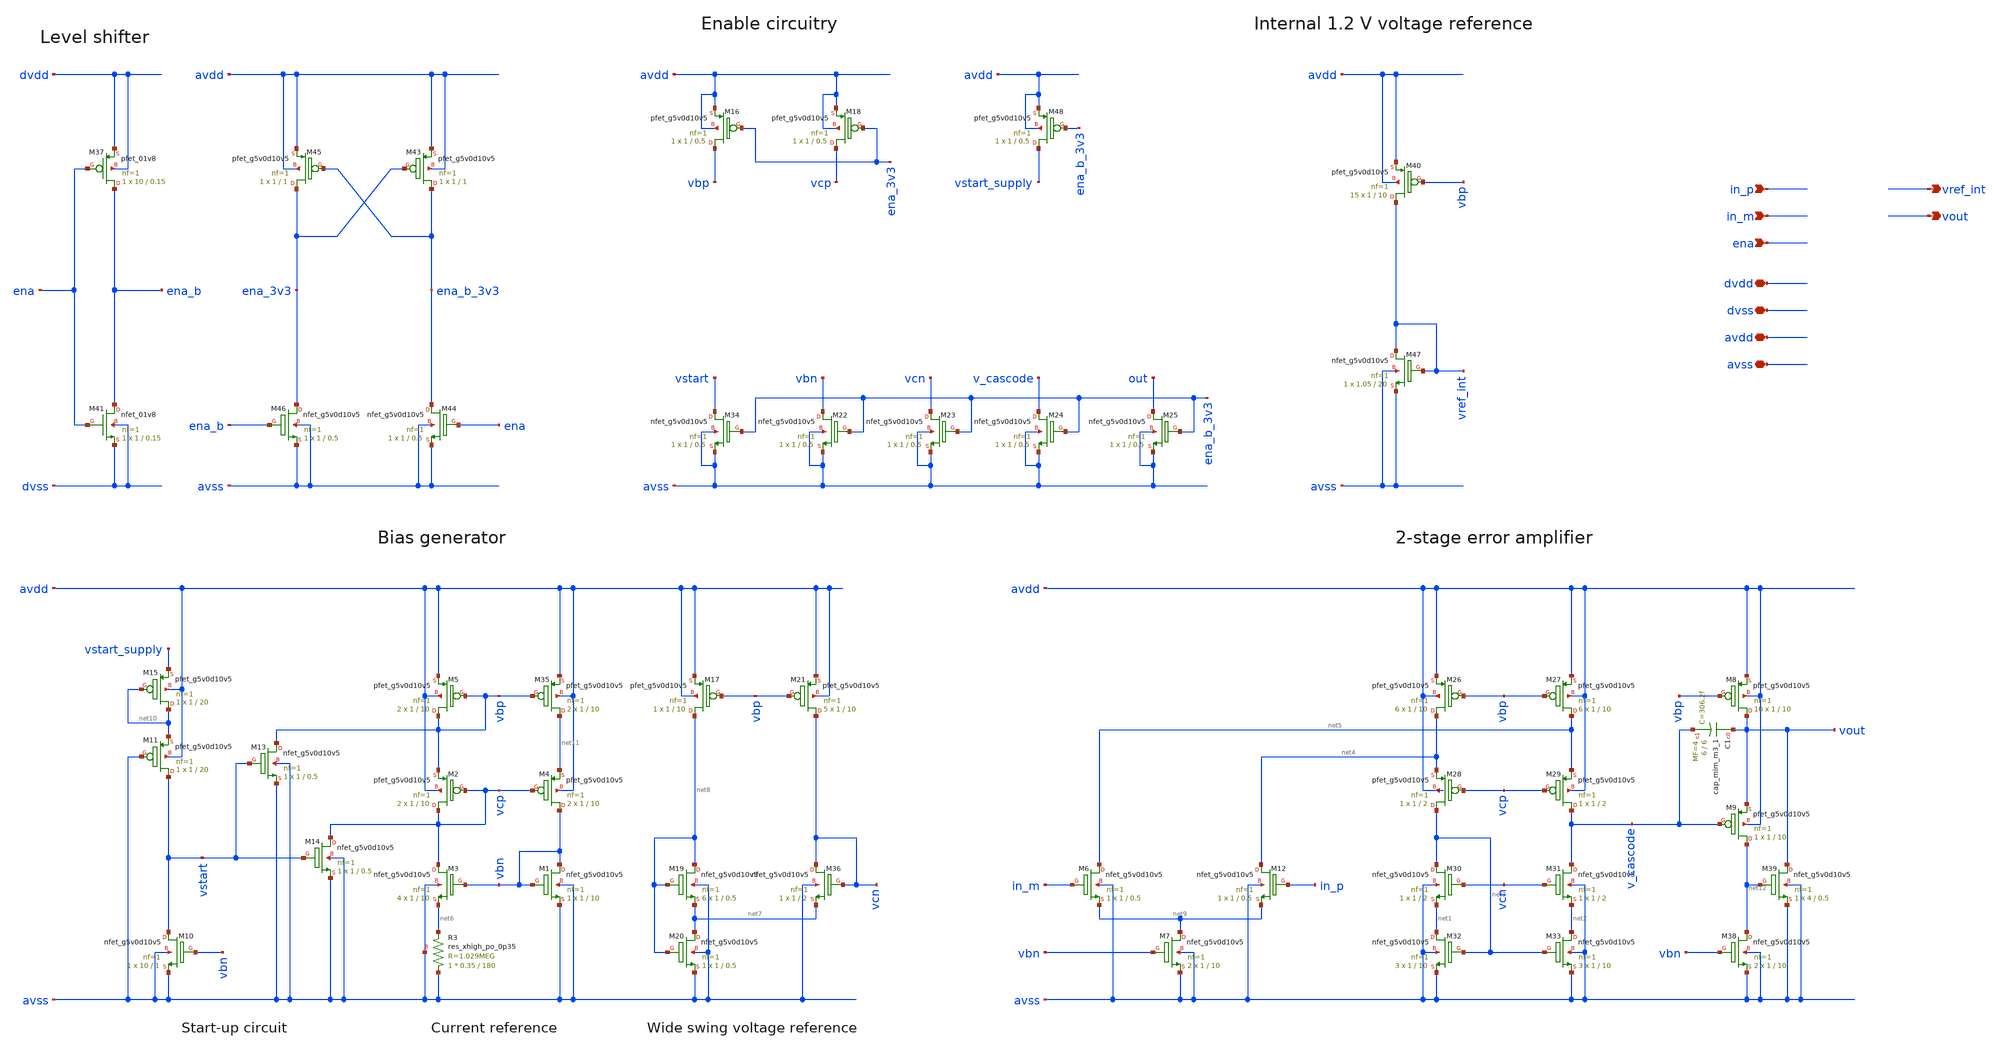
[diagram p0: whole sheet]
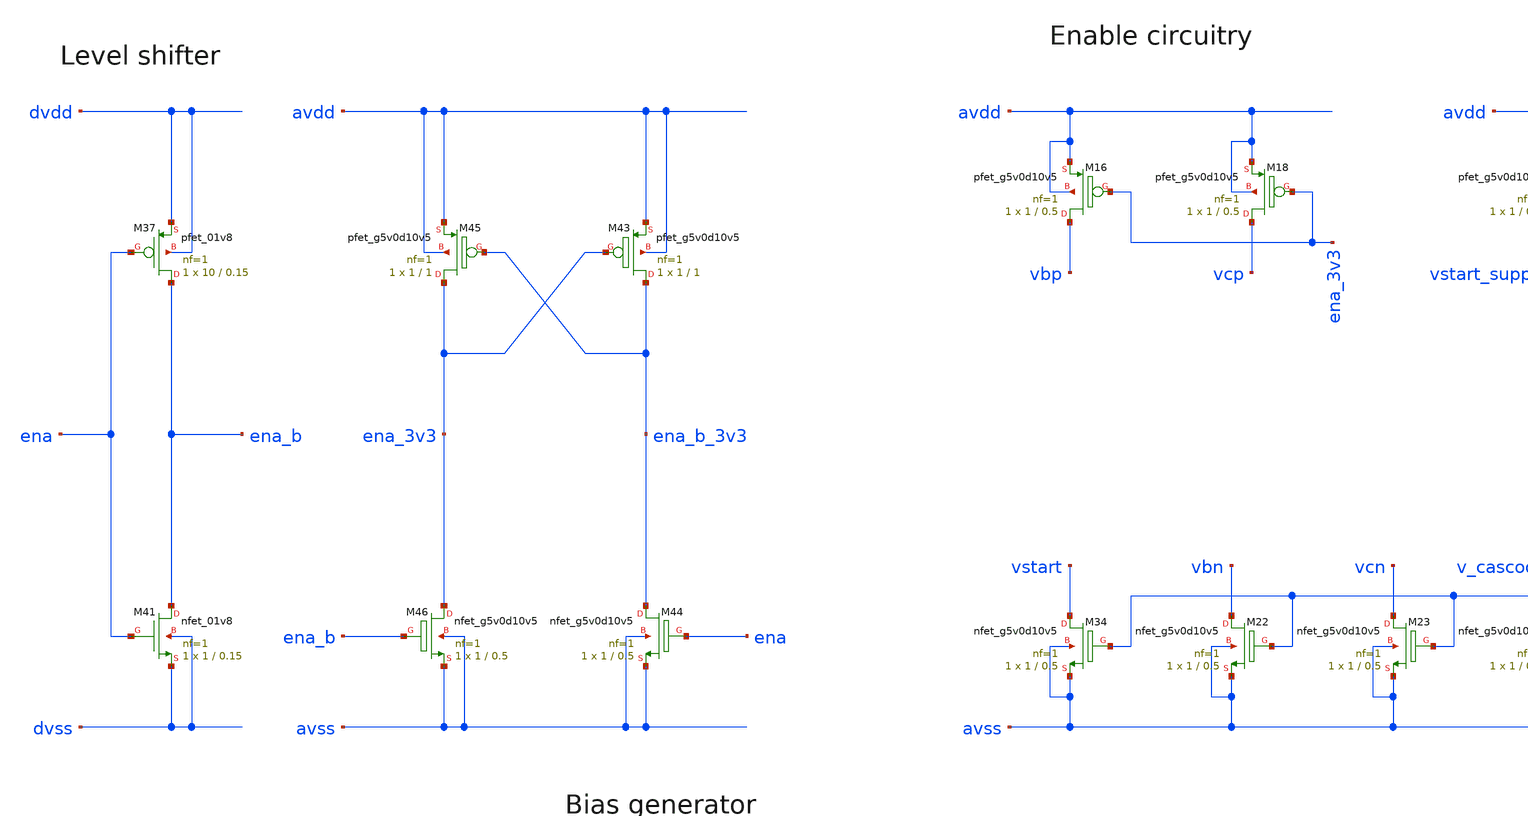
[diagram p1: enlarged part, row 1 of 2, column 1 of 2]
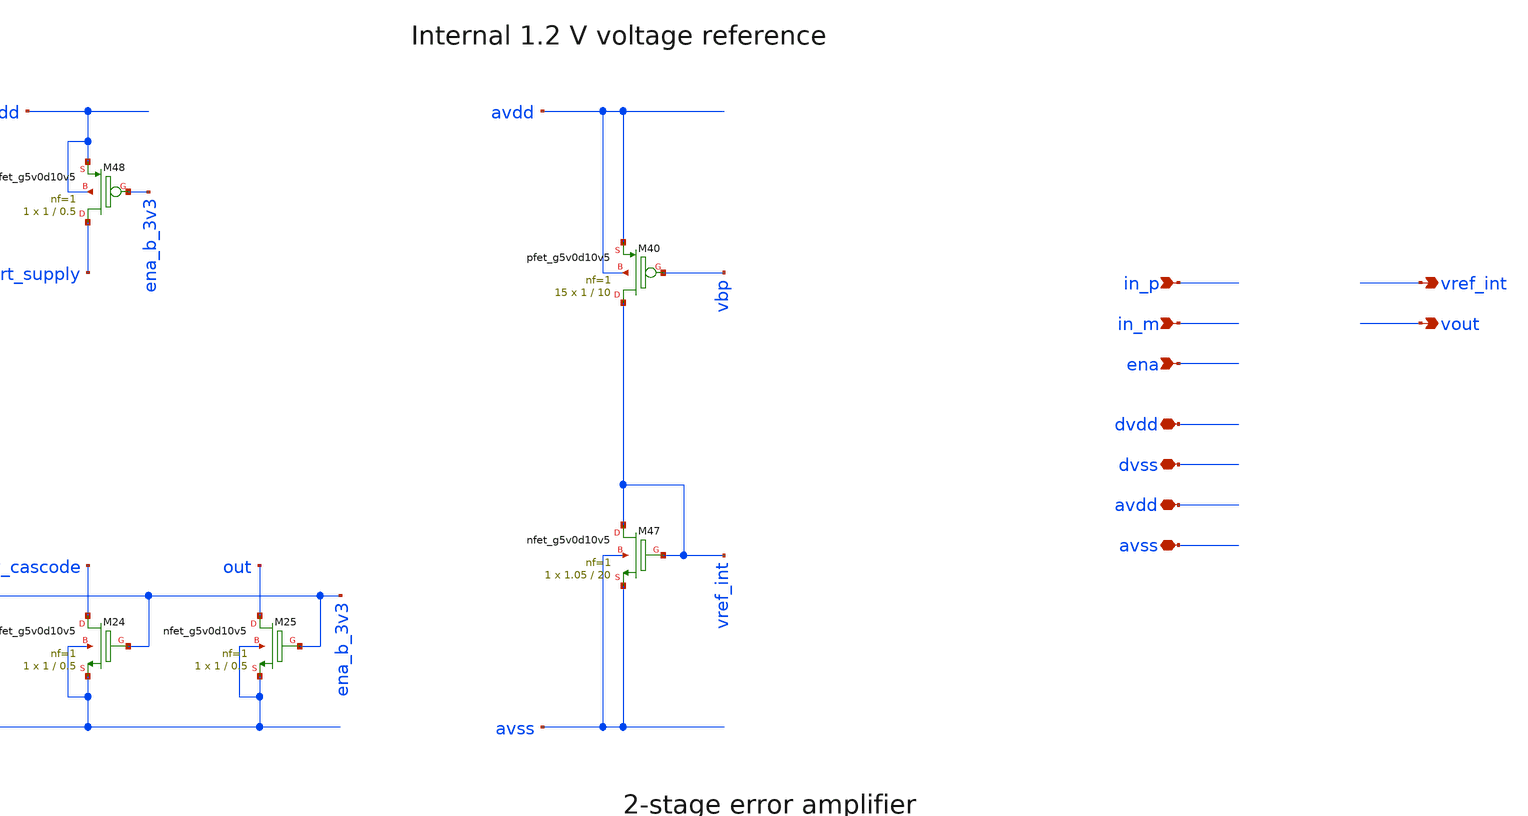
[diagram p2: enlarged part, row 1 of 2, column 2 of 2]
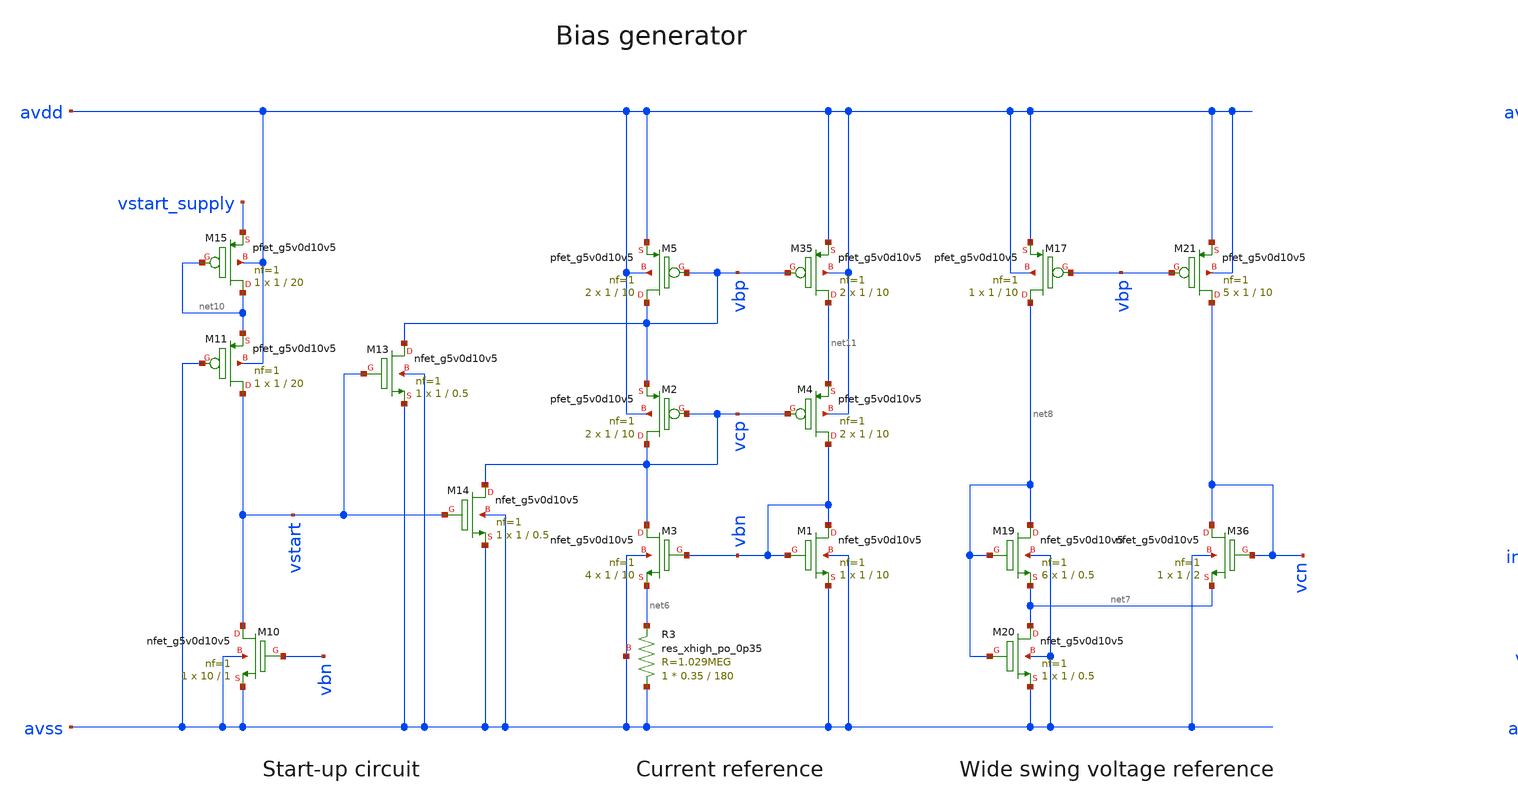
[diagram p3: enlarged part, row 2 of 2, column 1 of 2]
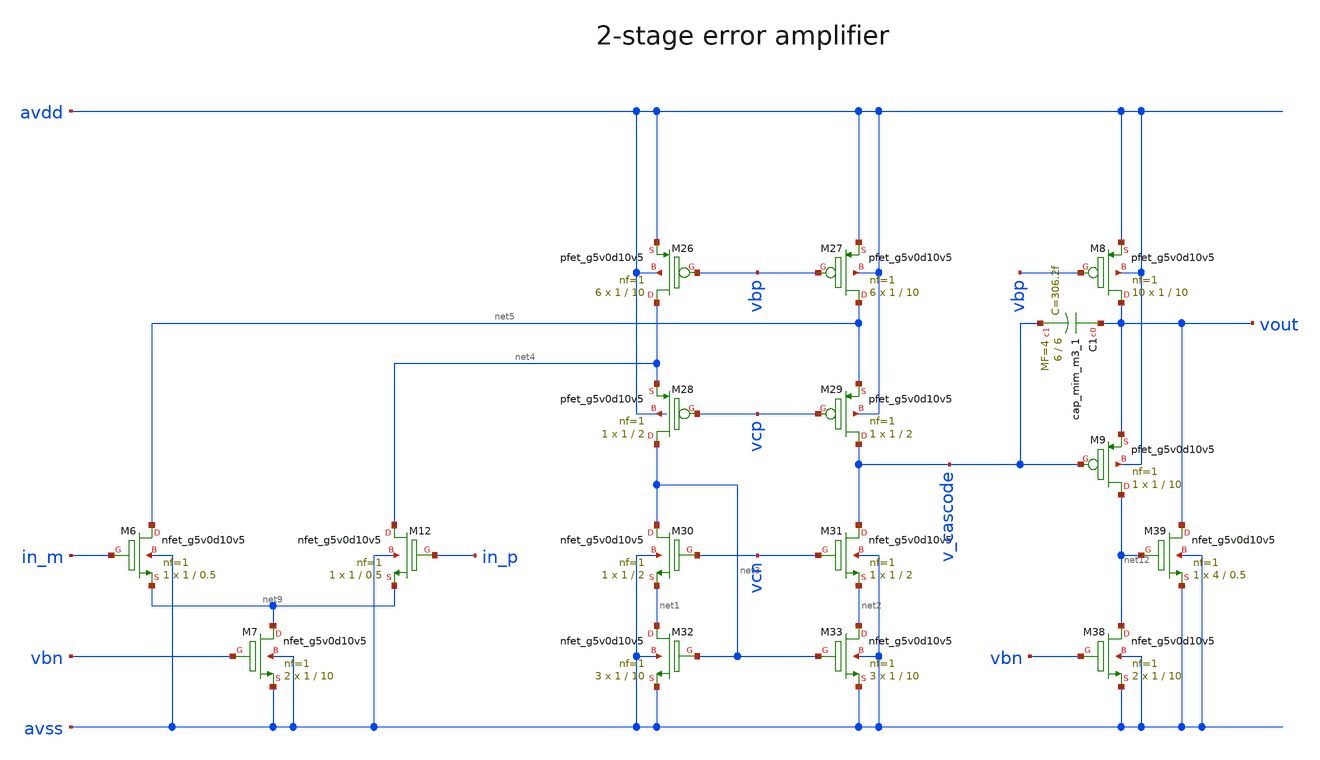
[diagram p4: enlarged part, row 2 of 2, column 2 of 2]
** sch_path: xschem/error_amplifier_03v3.sch
**.subckt error_amplifier_03v3 in_m in_p vout ena vref_int dvdd dvss avdd avss
*.ipin in_m
*.ipin in_p
*.opin vout
*.ipin ena
*.opin vref_int
*.iopin dvdd
*.iopin dvss
*.iopin avdd
*.iopin avss
XM1 vbn vbn avss avss sky130_fd_pr__nfet_g5v0d10v5 L=10 W=1 nf=1 ad='int((nf+1)/2) * W/nf * 0.29' as='int((nf+2)/2) * W/nf * 0.29'
+ pd='2*int((nf+1)/2) * (W/nf + 0.29)' ps='2*int((nf+2)/2) * (W/nf + 0.29)' nrd='0.29 / W' nrs='0.29 / W'
+ sa=0 sb=0 sd=0 mult=1 m=1
XM3 vcp vbn net6 avss sky130_fd_pr__nfet_g5v0d10v5 L=10 W=1 nf=1 ad='int((nf+1)/2) * W/nf * 0.29' as='int((nf+2)/2) * W/nf * 0.29'
+ pd='2*int((nf+1)/2) * (W/nf + 0.29)' ps='2*int((nf+2)/2) * (W/nf + 0.29)' nrd='0.29 / W' nrs='0.29 / W'
+ sa=0 sb=0 sd=0 mult=4 m=4
XM5 vbp vbp avdd avdd sky130_fd_pr__pfet_g5v0d10v5 L=10 W=1 nf=1 ad='int((nf+1)/2) * W/nf * 0.29' as='int((nf+2)/2) * W/nf * 0.29'
+ pd='2*int((nf+1)/2) * (W/nf + 0.29)' ps='2*int((nf+2)/2) * (W/nf + 0.29)' nrd='0.29 / W' nrs='0.29 / W'
+ sa=0 sb=0 sd=0 mult=2 m=2
XM26 net4 vbp avdd avdd sky130_fd_pr__pfet_g5v0d10v5 L=10 W=1 nf=1 ad='int((nf+1)/2) * W/nf * 0.29' as='int((nf+2)/2) * W/nf * 0.29'
+ pd='2*int((nf+1)/2) * (W/nf + 0.29)' ps='2*int((nf+2)/2) * (W/nf + 0.29)' nrd='0.29 / W' nrs='0.29 / W'
+ sa=0 sb=0 sd=0 mult=6 m=6
XM27 net5 vbp avdd avdd sky130_fd_pr__pfet_g5v0d10v5 L=10 W=1 nf=1 ad='int((nf+1)/2) * W/nf * 0.29' as='int((nf+2)/2) * W/nf * 0.29'
+ pd='2*int((nf+1)/2) * (W/nf + 0.29)' ps='2*int((nf+2)/2) * (W/nf + 0.29)' nrd='0.29 / W' nrs='0.29 / W'
+ sa=0 sb=0 sd=0 mult=6 m=6
XM28 net3 vcp net4 avdd sky130_fd_pr__pfet_g5v0d10v5 L=2 W=1 nf=1 ad='int((nf+1)/2) * W/nf * 0.29' as='int((nf+2)/2) * W/nf * 0.29'
+ pd='2*int((nf+1)/2) * (W/nf + 0.29)' ps='2*int((nf+2)/2) * (W/nf + 0.29)' nrd='0.29 / W' nrs='0.29 / W'
+ sa=0 sb=0 sd=0 mult=1 m=1
XM29 v_cascode vcp net5 avdd sky130_fd_pr__pfet_g5v0d10v5 L=2 W=1 nf=1 ad='int((nf+1)/2) * W/nf * 0.29'
+ as='int((nf+2)/2) * W/nf * 0.29' pd='2*int((nf+1)/2) * (W/nf + 0.29)' ps='2*int((nf+2)/2) * (W/nf + 0.29)'
+ nrd='0.29 / W' nrs='0.29 / W' sa=0 sb=0 sd=0 mult=1 m=1
XM30 net3 vcn net1 avss sky130_fd_pr__nfet_g5v0d10v5 L=2 W=1 nf=1 ad='int((nf+1)/2) * W/nf * 0.29' as='int((nf+2)/2) * W/nf * 0.29'
+ pd='2*int((nf+1)/2) * (W/nf + 0.29)' ps='2*int((nf+2)/2) * (W/nf + 0.29)' nrd='0.29 / W' nrs='0.29 / W'
+ sa=0 sb=0 sd=0 mult=1 m=1
XM31 v_cascode vcn net2 avss sky130_fd_pr__nfet_g5v0d10v5 L=2 W=1 nf=1 ad='int((nf+1)/2) * W/nf * 0.29'
+ as='int((nf+2)/2) * W/nf * 0.29' pd='2*int((nf+1)/2) * (W/nf + 0.29)' ps='2*int((nf+2)/2) * (W/nf + 0.29)'
+ nrd='0.29 / W' nrs='0.29 / W' sa=0 sb=0 sd=0 mult=1 m=1
XM32 net1 net3 avss avss sky130_fd_pr__nfet_g5v0d10v5 L=10 W=1 nf=1 ad='int((nf+1)/2) * W/nf * 0.29'
+ as='int((nf+2)/2) * W/nf * 0.29' pd='2*int((nf+1)/2) * (W/nf + 0.29)' ps='2*int((nf+2)/2) * (W/nf + 0.29)'
+ nrd='0.29 / W' nrs='0.29 / W' sa=0 sb=0 sd=0 mult=3 m=3
XM33 net2 net3 avss avss sky130_fd_pr__nfet_g5v0d10v5 L=10 W=1 nf=1 ad='int((nf+1)/2) * W/nf * 0.29'
+ as='int((nf+2)/2) * W/nf * 0.29' pd='2*int((nf+1)/2) * (W/nf + 0.29)' ps='2*int((nf+2)/2) * (W/nf + 0.29)'
+ nrd='0.29 / W' nrs='0.29 / W' sa=0 sb=0 sd=0 mult=3 m=3
XM35 net11 vbp avdd avdd sky130_fd_pr__pfet_g5v0d10v5 L=10 W=1 nf=1 ad='int((nf+1)/2) * W/nf * 0.29'
+ as='int((nf+2)/2) * W/nf * 0.29' pd='2*int((nf+1)/2) * (W/nf + 0.29)' ps='2*int((nf+2)/2) * (W/nf + 0.29)'
+ nrd='0.29 / W' nrs='0.29 / W' sa=0 sb=0 sd=0 mult=2 m=2
XR3 avss net6 avss sky130_fd_pr__res_xhigh_po_0p35 L=180 mult=1 m=1
XM9 net12 v_cascode vout avdd sky130_fd_pr__pfet_g5v0d10v5 L=10 W=1 nf=1 ad='int((nf+1)/2) * W/nf * 0.29'
+ as='int((nf+2)/2) * W/nf * 0.29' pd='2*int((nf+1)/2) * (W/nf + 0.29)' ps='2*int((nf+2)/2) * (W/nf + 0.29)'
+ nrd='0.29 / W' nrs='0.29 / W' sa=0 sb=0 sd=0 mult=1 m=1
XM8 vout vbp avdd avdd sky130_fd_pr__pfet_g5v0d10v5 L=10 W=1 nf=1 ad='int((nf+1)/2) * W/nf * 0.29' as='int((nf+2)/2) * W/nf * 0.29'
+ pd='2*int((nf+1)/2) * (W/nf + 0.29)' ps='2*int((nf+2)/2) * (W/nf + 0.29)' nrd='0.29 / W' nrs='0.29 / W'
+ sa=0 sb=0 sd=0 mult=10 m=10
XM17 net8 vbp avdd avdd sky130_fd_pr__pfet_g5v0d10v5 L=10 W=1 nf=1 ad='int((nf+1)/2) * W/nf * 0.29' as='int((nf+2)/2) * W/nf * 0.29'
+ pd='2*int((nf+1)/2) * (W/nf + 0.29)' ps='2*int((nf+2)/2) * (W/nf + 0.29)' nrd='0.29 / W' nrs='0.29 / W'
+ sa=0 sb=0 sd=0 mult=1 m=1
XM19 net8 net8 net7 avss sky130_fd_pr__nfet_g5v0d10v5 L=0.5 W=1 nf=1 ad='int((nf+1)/2) * W/nf * 0.29'
+ as='int((nf+2)/2) * W/nf * 0.29' pd='2*int((nf+1)/2) * (W/nf + 0.29)' ps='2*int((nf+2)/2) * (W/nf + 0.29)'
+ nrd='0.29 / W' nrs='0.29 / W' sa=0 sb=0 sd=0 mult=6 m=6
XM20 net7 net8 avss avss sky130_fd_pr__nfet_g5v0d10v5 L=0.5 W=1 nf=1 ad='int((nf+1)/2) * W/nf * 0.29'
+ as='int((nf+2)/2) * W/nf * 0.29' pd='2*int((nf+1)/2) * (W/nf + 0.29)' ps='2*int((nf+2)/2) * (W/nf + 0.29)'
+ nrd='0.29 / W' nrs='0.29 / W' sa=0 sb=0 sd=0 mult=1 m=1
XM21 vcn vbp avdd avdd sky130_fd_pr__pfet_g5v0d10v5 L=10 W=1 nf=1 ad='int((nf+1)/2) * W/nf * 0.29' as='int((nf+2)/2) * W/nf * 0.29'
+ pd='2*int((nf+1)/2) * (W/nf + 0.29)' ps='2*int((nf+2)/2) * (W/nf + 0.29)' nrd='0.29 / W' nrs='0.29 / W'
+ sa=0 sb=0 sd=0 mult=5 m=5
XM36 vcn vcn net7 avss sky130_fd_pr__nfet_g5v0d10v5 L=2 W=1 nf=1 ad='int((nf+1)/2) * W/nf * 0.29' as='int((nf+2)/2) * W/nf * 0.29'
+ pd='2*int((nf+1)/2) * (W/nf + 0.29)' ps='2*int((nf+2)/2) * (W/nf + 0.29)' nrd='0.29 / W' nrs='0.29 / W'
+ sa=0 sb=0 sd=0 mult=1 m=1
XM6 net5 in_m net9 avss sky130_fd_pr__nfet_g5v0d10v5 L=0.5 W=1 nf=1 ad='int((nf+1)/2) * W/nf * 0.29'
+ as='int((nf+2)/2) * W/nf * 0.29' pd='2*int((nf+1)/2) * (W/nf + 0.29)' ps='2*int((nf+2)/2) * (W/nf + 0.29)'
+ nrd='0.29 / W' nrs='0.29 / W' sa=0 sb=0 sd=0 mult=1 m=1
XM7 net9 vbn avss avss sky130_fd_pr__nfet_g5v0d10v5 L=10 W=1 nf=1 ad='int((nf+1)/2) * W/nf * 0.29' as='int((nf+2)/2) * W/nf * 0.29'
+ pd='2*int((nf+1)/2) * (W/nf + 0.29)' ps='2*int((nf+2)/2) * (W/nf + 0.29)' nrd='0.29 / W' nrs='0.29 / W'
+ sa=0 sb=0 sd=0 mult=2 m=2
XM12 net4 in_p net9 avss sky130_fd_pr__nfet_g5v0d10v5 L=0.5 W=1 nf=1 ad='int((nf+1)/2) * W/nf * 0.29'
+ as='int((nf+2)/2) * W/nf * 0.29' pd='2*int((nf+1)/2) * (W/nf + 0.29)' ps='2*int((nf+2)/2) * (W/nf + 0.29)'
+ nrd='0.29 / W' nrs='0.29 / W' sa=0 sb=0 sd=0 mult=1 m=1
XM10 vstart vbn avss avss sky130_fd_pr__nfet_g5v0d10v5 L=1 W=10 nf=1 ad='int((nf+1)/2) * W/nf * 0.29'
+ as='int((nf+2)/2) * W/nf * 0.29' pd='2*int((nf+1)/2) * (W/nf + 0.29)' ps='2*int((nf+2)/2) * (W/nf + 0.29)'
+ nrd='0.29 / W' nrs='0.29 / W' sa=0 sb=0 sd=0 mult=1 m=1
XM11 vstart avss net10 avdd sky130_fd_pr__pfet_g5v0d10v5 L=20 W=1 nf=1 ad='int((nf+1)/2) * W/nf * 0.29'
+ as='int((nf+2)/2) * W/nf * 0.29' pd='2*int((nf+1)/2) * (W/nf + 0.29)' ps='2*int((nf+2)/2) * (W/nf + 0.29)'
+ nrd='0.29 / W' nrs='0.29 / W' sa=0 sb=0 sd=0 mult=1 m=1
XM2 vcp vcp vbp avdd sky130_fd_pr__pfet_g5v0d10v5 L=10 W=1 nf=1 ad='int((nf+1)/2) * W/nf * 0.29' as='int((nf+2)/2) * W/nf * 0.29'
+ pd='2*int((nf+1)/2) * (W/nf + 0.29)' ps='2*int((nf+2)/2) * (W/nf + 0.29)' nrd='0.29 / W' nrs='0.29 / W'
+ sa=0 sb=0 sd=0 mult=2 m=2
XM4 vbn vcp net11 avdd sky130_fd_pr__pfet_g5v0d10v5 L=10 W=1 nf=1 ad='int((nf+1)/2) * W/nf * 0.29' as='int((nf+2)/2) * W/nf * 0.29'
+ pd='2*int((nf+1)/2) * (W/nf + 0.29)' ps='2*int((nf+2)/2) * (W/nf + 0.29)' nrd='0.29 / W' nrs='0.29 / W'
+ sa=0 sb=0 sd=0 mult=2 m=2
XM13 vbp vstart avss avss sky130_fd_pr__nfet_g5v0d10v5 L=0.5 W=1 nf=1 ad='int((nf+1)/2) * W/nf * 0.29'
+ as='int((nf+2)/2) * W/nf * 0.29' pd='2*int((nf+1)/2) * (W/nf + 0.29)' ps='2*int((nf+2)/2) * (W/nf + 0.29)'
+ nrd='0.29 / W' nrs='0.29 / W' sa=0 sb=0 sd=0 mult=1 m=1
XM14 vcp vstart avss avss sky130_fd_pr__nfet_g5v0d10v5 L=0.5 W=1 nf=1 ad='int((nf+1)/2) * W/nf * 0.29'
+ as='int((nf+2)/2) * W/nf * 0.29' pd='2*int((nf+1)/2) * (W/nf + 0.29)' ps='2*int((nf+2)/2) * (W/nf + 0.29)'
+ nrd='0.29 / W' nrs='0.29 / W' sa=0 sb=0 sd=0 mult=1 m=1
XM15 net10 net10 vstart_supply avdd sky130_fd_pr__pfet_g5v0d10v5 L=20 W=1 nf=1 ad='int((nf+1)/2) * W/nf * 0.29'
+ as='int((nf+2)/2) * W/nf * 0.29' pd='2*int((nf+1)/2) * (W/nf + 0.29)' ps='2*int((nf+2)/2) * (W/nf + 0.29)'
+ nrd='0.29 / W' nrs='0.29 / W' sa=0 sb=0 sd=0 mult=1 m=1
XM16 vbp ena_3v3 avdd avdd sky130_fd_pr__pfet_g5v0d10v5 L=0.5 W=1 nf=1 ad='int((nf+1)/2) * W/nf * 0.29'
+ as='int((nf+2)/2) * W/nf * 0.29' pd='2*int((nf+1)/2) * (W/nf + 0.29)' ps='2*int((nf+2)/2) * (W/nf + 0.29)'
+ nrd='0.29 / W' nrs='0.29 / W' sa=0 sb=0 sd=0 mult=1 m=1
XM18 vcp ena_3v3 avdd avdd sky130_fd_pr__pfet_g5v0d10v5 L=0.5 W=1 nf=1 ad='int((nf+1)/2) * W/nf * 0.29'
+ as='int((nf+2)/2) * W/nf * 0.29' pd='2*int((nf+1)/2) * (W/nf + 0.29)' ps='2*int((nf+2)/2) * (W/nf + 0.29)'
+ nrd='0.29 / W' nrs='0.29 / W' sa=0 sb=0 sd=0 mult=1 m=1
XM22 vbn ena_b_3v3 avss avss sky130_fd_pr__nfet_g5v0d10v5 L=0.5 W=1 nf=1 ad='int((nf+1)/2) * W/nf * 0.29'
+ as='int((nf+2)/2) * W/nf * 0.29' pd='2*int((nf+1)/2) * (W/nf + 0.29)' ps='2*int((nf+2)/2) * (W/nf + 0.29)'
+ nrd='0.29 / W' nrs='0.29 / W' sa=0 sb=0 sd=0 mult=1 m=1
XM23 vcn ena_b_3v3 avss avss sky130_fd_pr__nfet_g5v0d10v5 L=0.5 W=1 nf=1 ad='int((nf+1)/2) * W/nf * 0.29'
+ as='int((nf+2)/2) * W/nf * 0.29' pd='2*int((nf+1)/2) * (W/nf + 0.29)' ps='2*int((nf+2)/2) * (W/nf + 0.29)'
+ nrd='0.29 / W' nrs='0.29 / W' sa=0 sb=0 sd=0 mult=1 m=1
XM24 v_cascode ena_b_3v3 avss avss sky130_fd_pr__nfet_g5v0d10v5 L=0.5 W=1 nf=1 ad='int((nf+1)/2) * W/nf * 0.29'
+ as='int((nf+2)/2) * W/nf * 0.29' pd='2*int((nf+1)/2) * (W/nf + 0.29)' ps='2*int((nf+2)/2) * (W/nf + 0.29)'
+ nrd='0.29 / W' nrs='0.29 / W' sa=0 sb=0 sd=0 mult=1 m=1
XM25 out ena_b_3v3 avss avss sky130_fd_pr__nfet_g5v0d10v5 L=0.5 W=1 nf=1 ad='int((nf+1)/2) * W/nf * 0.29'
+ as='int((nf+2)/2) * W/nf * 0.29' pd='2*int((nf+1)/2) * (W/nf + 0.29)' ps='2*int((nf+2)/2) * (W/nf + 0.29)'
+ nrd='0.29 / W' nrs='0.29 / W' sa=0 sb=0 sd=0 mult=1 m=1
XM34 vstart ena_b_3v3 avss avss sky130_fd_pr__nfet_g5v0d10v5 L=0.5 W=1 nf=1 ad='int((nf+1)/2) * W/nf * 0.29'
+ as='int((nf+2)/2) * W/nf * 0.29' pd='2*int((nf+1)/2) * (W/nf + 0.29)' ps='2*int((nf+2)/2) * (W/nf + 0.29)'
+ nrd='0.29 / W' nrs='0.29 / W' sa=0 sb=0 sd=0 mult=1 m=1
XM38 net12 vbn avss avss sky130_fd_pr__nfet_g5v0d10v5 L=10 W=1 nf=1 ad='int((nf+1)/2) * W/nf * 0.29'
+ as='int((nf+2)/2) * W/nf * 0.29' pd='2*int((nf+1)/2) * (W/nf + 0.29)' ps='2*int((nf+2)/2) * (W/nf + 0.29)'
+ nrd='0.29 / W' nrs='0.29 / W' sa=0 sb=0 sd=0 mult=2 m=2
XM39 vout net12 avss avss sky130_fd_pr__nfet_g5v0d10v5 L=0.5 W=4 nf=1 ad='int((nf+1)/2) * W/nf * 0.29'
+ as='int((nf+2)/2) * W/nf * 0.29' pd='2*int((nf+1)/2) * (W/nf + 0.29)' ps='2*int((nf+2)/2) * (W/nf + 0.29)'
+ nrd='0.29 / W' nrs='0.29 / W' sa=0 sb=0 sd=0 mult=1 m=1
XM43 ena_b_3v3 ena_3v3 avdd avdd sky130_fd_pr__pfet_g5v0d10v5 L=1 W=1 nf=1 ad='int((nf+1)/2) * W/nf * 0.29'
+ as='int((nf+2)/2) * W/nf * 0.29' pd='2*int((nf+1)/2) * (W/nf + 0.29)' ps='2*int((nf+2)/2) * (W/nf + 0.29)'
+ nrd='0.29 / W' nrs='0.29 / W' sa=0 sb=0 sd=0 mult=1 m=1
XM44 ena_b_3v3 ena avss avss sky130_fd_pr__nfet_g5v0d10v5 L=0.5 W=1 nf=1 ad='int((nf+1)/2) * W/nf * 0.29'
+ as='int((nf+2)/2) * W/nf * 0.29' pd='2*int((nf+1)/2) * (W/nf + 0.29)' ps='2*int((nf+2)/2) * (W/nf + 0.29)'
+ nrd='0.29 / W' nrs='0.29 / W' sa=0 sb=0 sd=0 mult=1 m=1
XM45 ena_3v3 ena_b_3v3 avdd avdd sky130_fd_pr__pfet_g5v0d10v5 L=1 W=1 nf=1 ad='int((nf+1)/2) * W/nf * 0.29'
+ as='int((nf+2)/2) * W/nf * 0.29' pd='2*int((nf+1)/2) * (W/nf + 0.29)' ps='2*int((nf+2)/2) * (W/nf + 0.29)'
+ nrd='0.29 / W' nrs='0.29 / W' sa=0 sb=0 sd=0 mult=1 m=1
XM46 ena_3v3 ena_b avss avss sky130_fd_pr__nfet_g5v0d10v5 L=0.5 W=1 nf=1 ad='int((nf+1)/2) * W/nf * 0.29'
+ as='int((nf+2)/2) * W/nf * 0.29' pd='2*int((nf+1)/2) * (W/nf + 0.29)' ps='2*int((nf+2)/2) * (W/nf + 0.29)'
+ nrd='0.29 / W' nrs='0.29 / W' sa=0 sb=0 sd=0 mult=1 m=1
XC1 vout v_cascode sky130_fd_pr__cap_mim_m3_1 W=6 L=6 MF=4 m=4
XM40 vref_int vbp avdd avdd sky130_fd_pr__pfet_g5v0d10v5 L=10 W=1 nf=1 ad='int((nf+1)/2) * W/nf * 0.29'
+ as='int((nf+2)/2) * W/nf * 0.29' pd='2*int((nf+1)/2) * (W/nf + 0.29)' ps='2*int((nf+2)/2) * (W/nf + 0.29)'
+ nrd='0.29 / W' nrs='0.29 / W' sa=0 sb=0 sd=0 mult=15 m=15
XM47 vref_int vref_int avss avss sky130_fd_pr__nfet_g5v0d10v5 L=20 W=1.05 nf=1 ad='int((nf+1)/2) * W/nf * 0.29'
+ as='int((nf+2)/2) * W/nf * 0.29' pd='2*int((nf+1)/2) * (W/nf + 0.29)' ps='2*int((nf+2)/2) * (W/nf + 0.29)'
+ nrd='0.29 / W' nrs='0.29 / W' sa=0 sb=0 sd=0 mult=1 m=1
XM48 vstart_supply ena_b_3v3 avdd avdd sky130_fd_pr__pfet_g5v0d10v5 L=0.5 W=1 nf=1 ad='int((nf+1)/2) * W/nf * 0.29'
+ as='int((nf+2)/2) * W/nf * 0.29' pd='2*int((nf+1)/2) * (W/nf + 0.29)' ps='2*int((nf+2)/2) * (W/nf + 0.29)'
+ nrd='0.29 / W' nrs='0.29 / W' sa=0 sb=0 sd=0 mult=1 m=1
XM41 ena_b ena dvss dvss sky130_fd_pr__nfet_01v8 L=0.15 W=1 nf=1 ad='int((nf+1)/2) * W/nf * 0.29' as='int((nf+2)/2) * W/nf * 0.29'
+ pd='2*int((nf+1)/2) * (W/nf + 0.29)' ps='2*int((nf+2)/2) * (W/nf + 0.29)' nrd='0.29 / W' nrs='0.29 / W'
+ sa=0 sb=0 sd=0 mult=1 m=1
XM37 ena_b ena dvdd dvdd sky130_fd_pr__pfet_01v8 L=0.15 W=10 nf=1 ad='int((nf+1)/2) * W/nf * 0.29' as='int((nf+2)/2) * W/nf * 0.29'
+ pd='2*int((nf+1)/2) * (W/nf + 0.29)' ps='2*int((nf+2)/2) * (W/nf + 0.29)' nrd='0.29 / W' nrs='0.29 / W'
+ sa=0 sb=0 sd=0 mult=1 m=1
**.ends
.end
